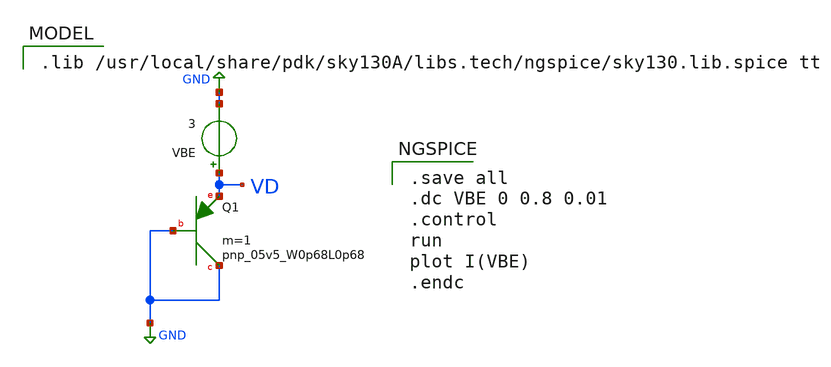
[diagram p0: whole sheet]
** sch_path: 1_diode_0p68_IV_curve.sch
**.subckt 1_diode_0p68_IV_curve
XQ1 GND GND VD sky130_fd_pr__pnp_05v5_W0p68L0p68 m=1
VBE VD GND 3
**** begin user architecture code

.save all
.dc VBE 0 0.8 0.01
.control
run
plot I(VBE)
.endc


.lib /usr/local/share/pdk/sky130A/libs.tech/ngspice/sky130.lib.spice tt

**** end user architecture code
**.ends
.GLOBAL GND
.end
